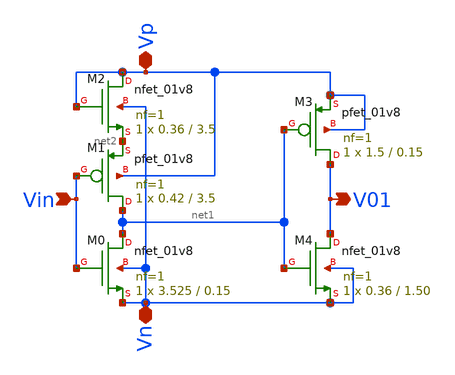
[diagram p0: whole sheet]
** sch_path: xschem/Vth_sch/Symbol/th01.sch
**.subckt th01 Vin V01 Vp Vn
*.ipin Vin
*.opin V01
*.iopin Vp
*.iopin Vn
XM3 V01 net1 Vp Vp sky130_fd_pr__pfet_01v8 L=0.15 W=1.5 nf=1 ad='int((nf+1)/2) * W/nf * 0.29' as='int((nf+2)/2) * W/nf * 0.29'
+ pd='2*int((nf+1)/2) * (W/nf + 0.29)' ps='2*int((nf+2)/2) * (W/nf + 0.29)' nrd='0.29 / W' nrs='0.29 / W'
+ sa=0 sb=0 sd=0 mult=1 m=1
XM4 V01 net1 Vn Vn sky130_fd_pr__nfet_01v8 L=1.50 W=0.36 nf=1 ad='int((nf+1)/2) * W/nf * 0.29' as='int((nf+2)/2) * W/nf * 0.29'
+ pd='2*int((nf+1)/2) * (W/nf + 0.29)' ps='2*int((nf+2)/2) * (W/nf + 0.29)' nrd='0.29 / W' nrs='0.29 / W'
+ sa=0 sb=0 sd=0 mult=1 m=1
XM1 net1 Vin net2 Vp sky130_fd_pr__pfet_01v8 L=3.5 W=0.42 nf=1 ad='int((nf+1)/2) * W/nf * 0.29' as='int((nf+2)/2) * W/nf * 0.29'
+ pd='2*int((nf+1)/2) * (W/nf + 0.29)' ps='2*int((nf+2)/2) * (W/nf + 0.29)' nrd='0.29 / W' nrs='0.29 / W'
+ sa=0 sb=0 sd=0 mult=1 m=1
XM0 net1 Vin Vn Vn sky130_fd_pr__nfet_01v8 L=0.15 W=3.525 nf=1 ad='int((nf+1)/2) * W/nf * 0.29' as='int((nf+2)/2) * W/nf * 0.29'
+ pd='2*int((nf+1)/2) * (W/nf + 0.29)' ps='2*int((nf+2)/2) * (W/nf + 0.29)' nrd='0.29 / W' nrs='0.29 / W'
+ sa=0 sb=0 sd=0 mult=1 m=1
XM2 Vp Vp net2 Vn sky130_fd_pr__nfet_01v8 L=3.5 W=0.36 nf=1 ad='int((nf+1)/2) * W/nf * 0.29' as='int((nf+2)/2) * W/nf * 0.29'
+ pd='2*int((nf+1)/2) * (W/nf + 0.29)' ps='2*int((nf+2)/2) * (W/nf + 0.29)' nrd='0.29 / W' nrs='0.29 / W'
+ sa=0 sb=0 sd=0 mult=1 m=1
**.ends
.end
